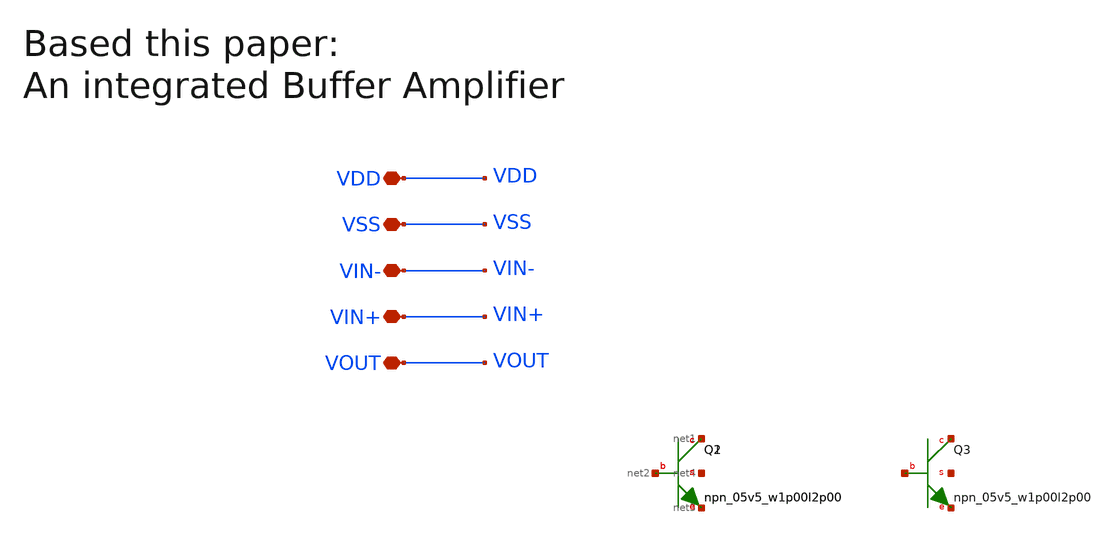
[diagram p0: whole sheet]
** sch_path: my_ip/LIB/Sky130A/single ended amplifiers/BIP001_PMOS_5_sky130A.sch
**.subckt BIP001_PMOS_5_sky130A VDD VSS VIN- VIN+ VOUT
*.iopin VDD
*.iopin VSS
*.iopin VIN-
*.iopin VIN+
*.iopin VOUT
XQ2 net1 net2 net3 net4 sky130_fd_pr__npn_05v5_w1p00l2p00
XQ1 net1 net2 net3 net4 sky130_fd_pr__npn_05v5_w1p00l2p00
XQ3 net5 net6 net7 net8 sky130_fd_pr__npn_05v5_w1p00l2p00
**.ends
.end
